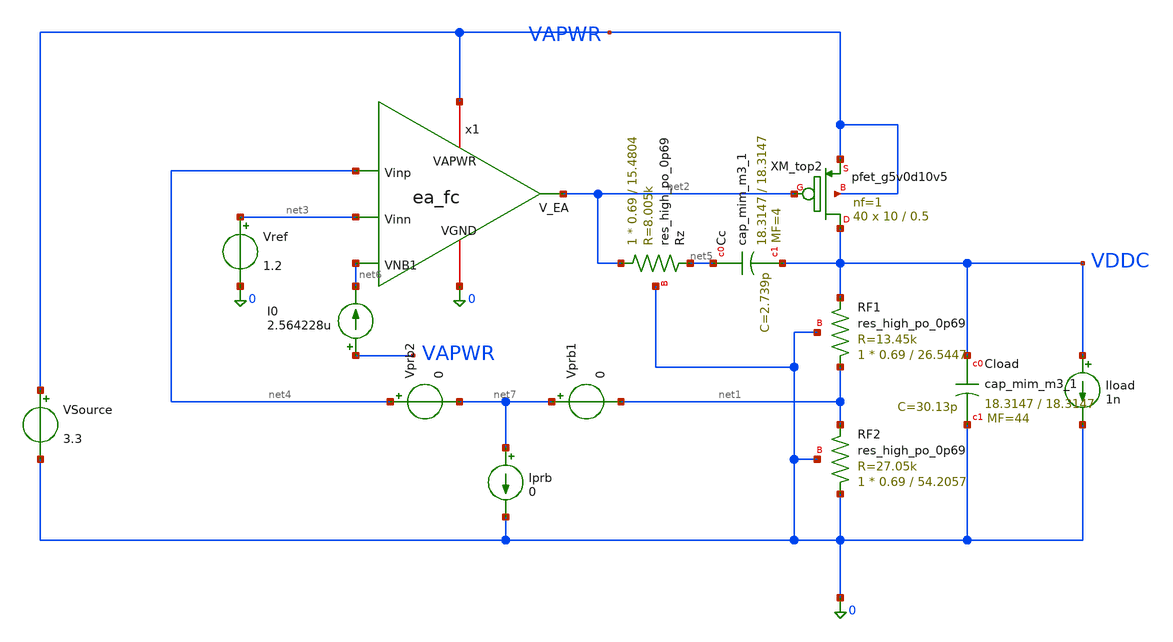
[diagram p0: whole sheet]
** sch_path: designs/bgr_ldo/ldo/ldo_core_tb.sch
**.subckt ldo_core_tb
Vref net3 0 1.2
XXM_top2 VDDC net2 VAPWR VAPWR sky130_fd_pr__pfet_g5v0d10v5 L=0.5 W=10 nf=1 ad='int((1 + 1)/2) * 10 / 1 * 0.29'
+ as='int((1 + 2)/2) * 10 / 1 * 0.29' pd='2*int((1 + 1)/2) * (10 / 1 + 0.29)' ps='2*int((1 + 2)/2) * (10 / 1 + 0.29)'
+ nrd='0.29 / 10 ' nrs='0.29 / 10 ' sa=0 sb=0 sd=0 mult=40 m=40
VSource VAPWR 0 3.3
x1 VAPWR net2 net4 net3 net6 0 ea_fc
Iload VDDC 0 1n
I0 VAPWR net6 2.564228u
XRF1 net1 VDDC 0 sky130_fd_pr__res_high_po_0p69 L=26.5447 mult=1 m=1
XRF2 0 net1 0 sky130_fd_pr__res_high_po_0p69 L=54.2057 mult=1 m=1
XRz net2 net5 0 sky130_fd_pr__res_high_po_0p69 L=15.4804 mult=1 m=1
XCload VDDC 0 sky130_fd_pr__cap_mim_m3_1 W=18.3147 L=18.3147 MF=44 m=44
XCc net5 VDDC sky130_fd_pr__cap_mim_m3_1 W=18.3147 L=18.3147 MF=4 m=4
Vprb1 net7 net1 0
Vprb2 net4 net7 0
Iprb net7 0 0
**.ends
.end
